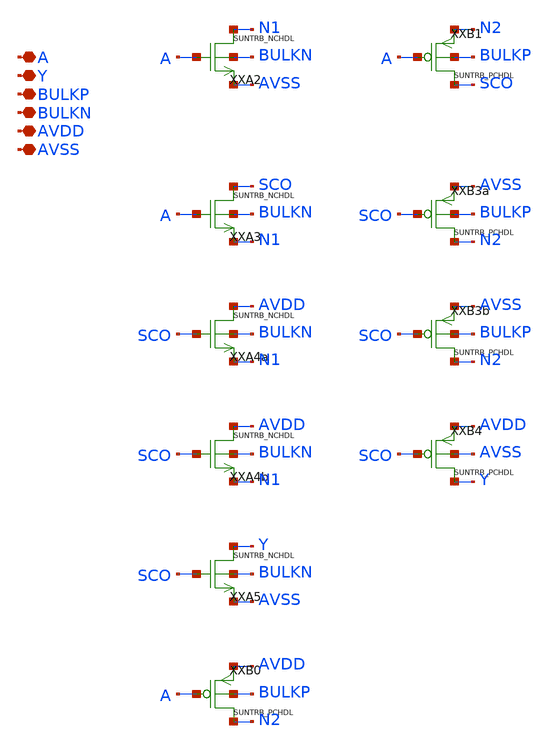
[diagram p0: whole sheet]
** sch_path: design/SUN_TRB_SKY130NM/SUNTRB_SCX1_CV.sch
**.subckt SUNTRB_SCX1_CV A Y BULKP BULKN AVDD AVSS
*.iopin A
*.iopin Y
*.iopin BULKP
*.iopin BULKN
*.iopin AVDD
*.iopin AVSS
XXA2 N1 A AVSS BULKN SUNTRB_NCHDL xoffset=0 yoffset=0 angle=0
XXA3 SCO A N1 BULKN SUNTRB_NCHDL xoffset=0 yoffset=0 angle=0
XXA4a AVDD SCO N1 BULKN SUNTRB_NCHDL xoffset=0 yoffset=0 angle=0
XXA4b AVDD SCO N1 BULKN SUNTRB_NCHDL xoffset=0 yoffset=0 angle=0
XXA5 Y SCO AVSS BULKN SUNTRB_NCHDL xoffset=0 yoffset=0 angle=0
XXB0 N2 A AVDD BULKP SUNTRB_PCHDL xoffset=0 yoffset=0 angle=0 M=1
XXB1 SCO A N2 BULKP SUNTRB_PCHDL xoffset=0 yoffset=0 angle=0 M=1
XXB3a N2 SCO AVSS BULKP SUNTRB_PCHDL xoffset=0 yoffset=0 angle=0 M=1
XXB3b N2 SCO AVSS BULKP SUNTRB_PCHDL xoffset=0 yoffset=0 angle=0 M=1
XXB4 Y SCO AVDD AVSS SUNTRB_PCHDL xoffset=0 yoffset=0 angle=0 M=1
**.ends
.end
